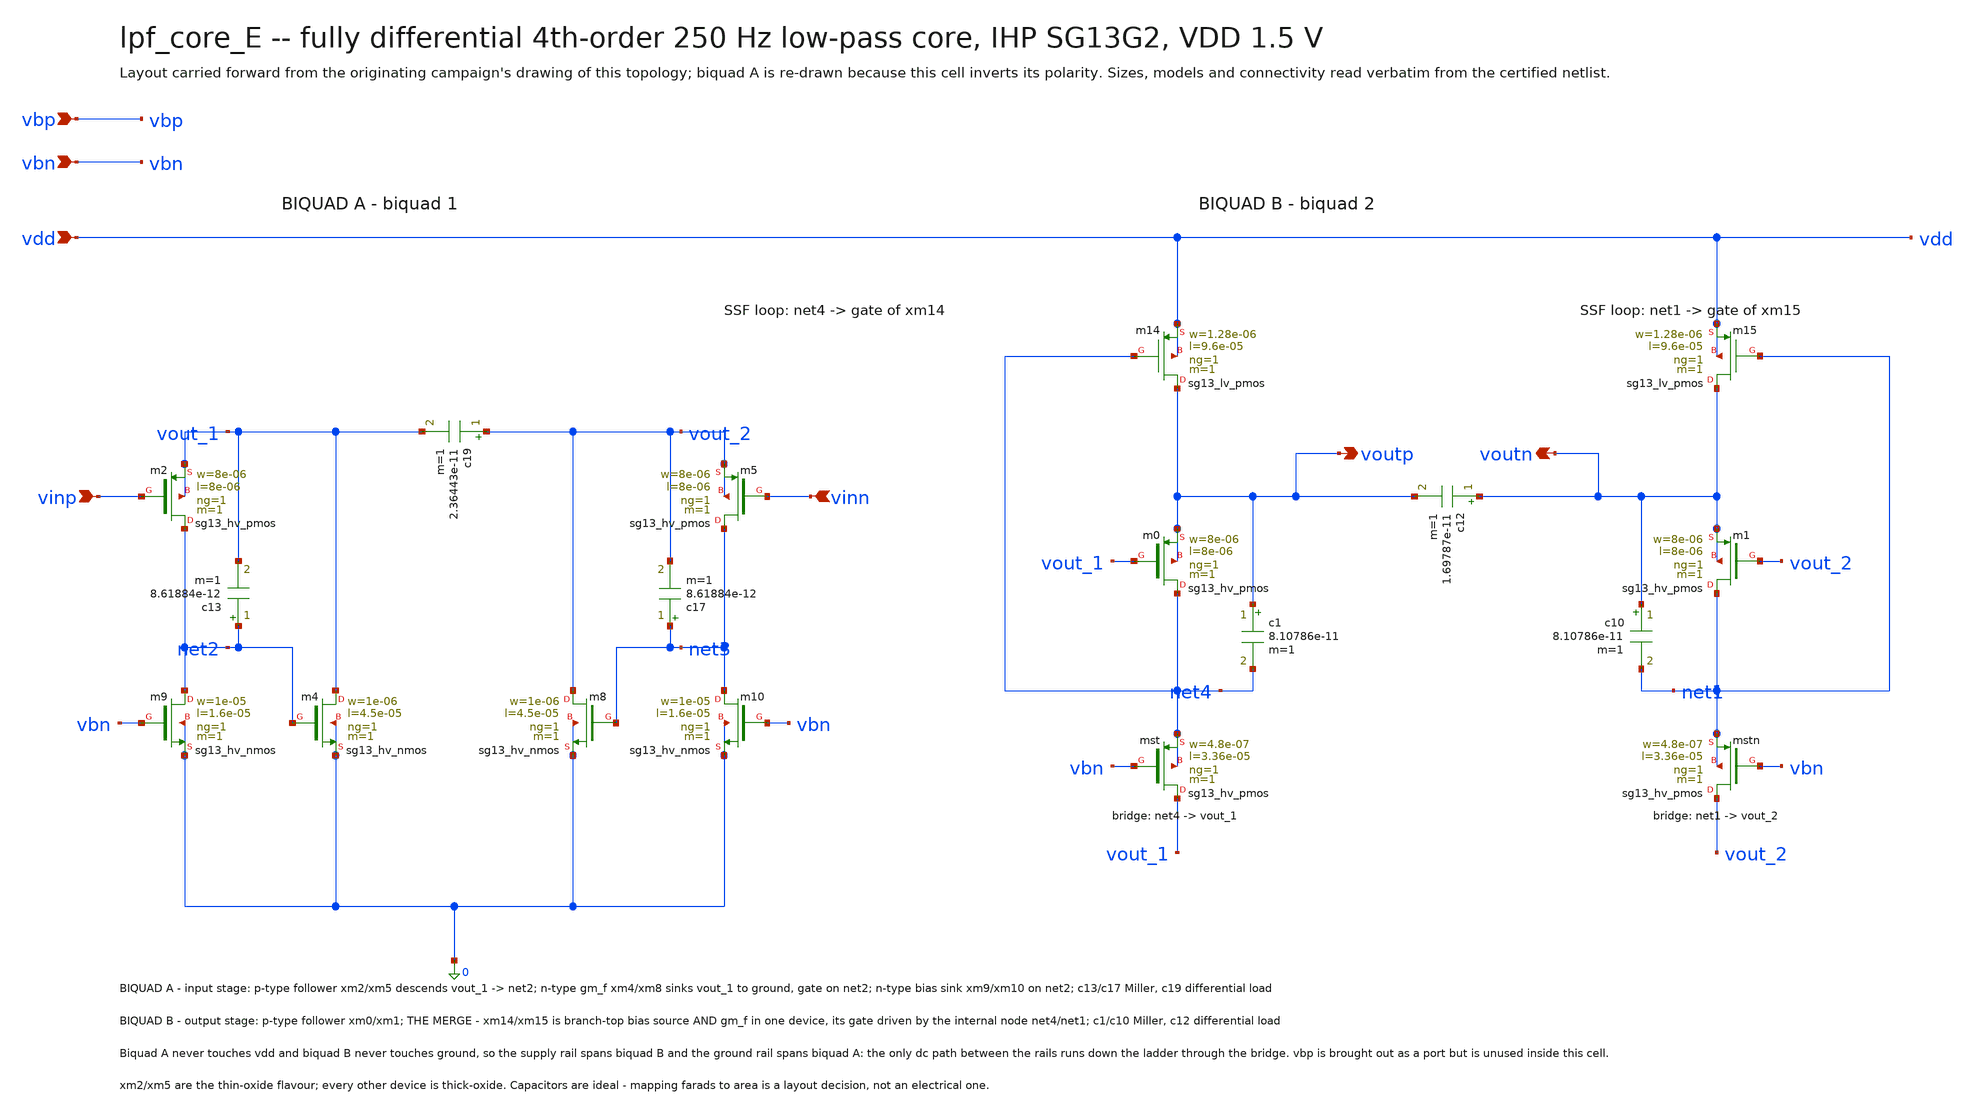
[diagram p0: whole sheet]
** sch_path: signoff/E-combo/lpf_core_E.sch
**.subckt lpf_core_E vinp vinn voutp voutn vdd vbn vbp
*.ipin vinp
*.ipin vinn
*.opin voutp
*.opin voutn
*.ipin vdd
*.ipin vbn
*.ipin vbp
Xm2 net2 vinp vout_1 vout_1 sg13_hv_pmos w=8e-06 l=8e-06 ng=1 m=1 mm_ok=1
Xm5 net3 vinn vout_2 vout_2 sg13_hv_pmos w=8e-06 l=8e-06 ng=1 m=1 mm_ok=1
Xm4 vout_1 net2 0 0 sg13_hv_nmos w=1e-06 l=4.5e-05 ng=1 m=1 mm_ok=1
Xm8 vout_2 net3 0 0 sg13_hv_nmos w=1e-06 l=4.5e-05 ng=1 m=1 mm_ok=1
Xm9 net2 vbn 0 0 sg13_hv_nmos w=1e-05 l=1.6e-05 ng=1 m=1 mm_ok=1
Xm10 net3 vbn 0 0 sg13_hv_nmos w=1e-05 l=1.6e-05 ng=1 m=1 mm_ok=1
Xmst vout_1 vbn net4 net4 sg13_hv_pmos w=4.8e-07 l=3.36e-05 ng=1 m=1 mm_ok=1
Xmstn vout_2 vbn net1 net1 sg13_hv_pmos w=4.8e-07 l=3.36e-05 ng=1 m=1 mm_ok=1
Xm0 net4 vout_1 voutp voutp sg13_hv_pmos w=8e-06 l=8e-06 ng=1 m=1 mm_ok=1
Xm1 net1 vout_2 voutn voutn sg13_hv_pmos w=8e-06 l=8e-06 ng=1 m=1 mm_ok=1
Xm14 voutp net4 vdd vdd sg13_lv_pmos w=1.28e-06 l=9.6e-05 ng=1 m=1 mm_ok=1
Xm15 voutn net1 vdd vdd sg13_lv_pmos w=1.28e-06 l=9.6e-05 ng=1 m=1 mm_ok=1
c13 net2 vout_1 8.61884e-12 m=1
c17 net3 vout_2 8.61884e-12 m=1
c19 vout_2 vout_1 2.36443e-11 m=1
c1 voutp net4 8.10786e-11 m=1
c10 voutn net1 8.10786e-11 m=1
c12 voutn voutp 1.69787e-11 m=1
**.ends
.end
